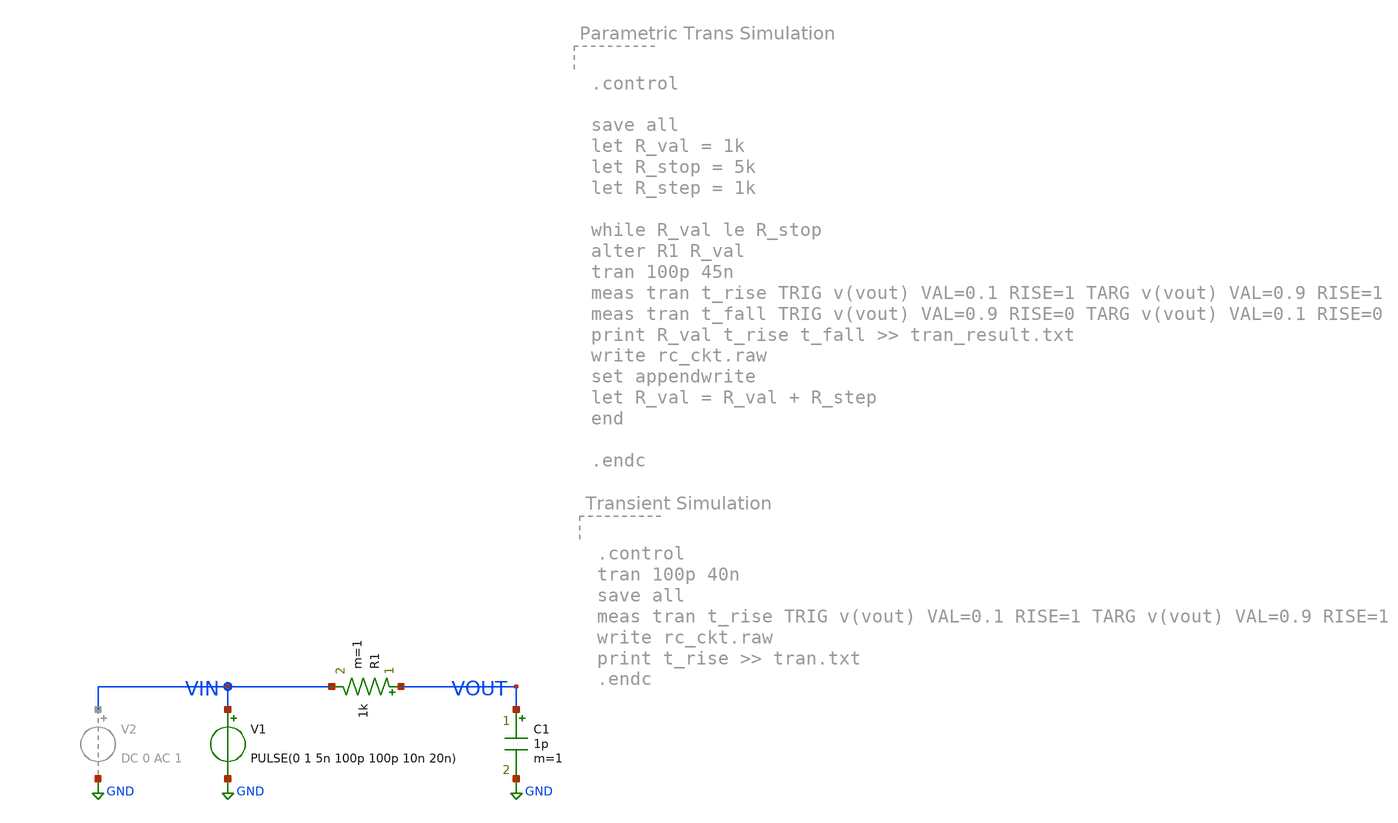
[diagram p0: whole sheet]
** sch_path: ITI_Labs/Lab1/RC/Design/RC.sch
**.subckt RC
C1 VOUT GND 1p m=1
R1 VOUT VIN 1k m=1
V1 VIN GND PULSE(0 1 5n 100p 100p 10n 20n)
**** begin user architecture code


.control

save all

let R_val = 1k
let R_stop = 1meg
let R_mult = 10

while R_val le R_stop
alter R1 R_val
ac dec 10 1 10g

meas ac MAX_GAIN MAX vmag(vout) FROM=1 TO=10G
meas ac BW WHEN vmag(vout)=0.707 FALL=1

print MAX_GAIN BW >> ac_result.txt
write rc_ckt_2.raw
set appendwrite
let R_val = R_val * R_mult
end

.endc




.control
ac dec 10 1 10G
save all
meas ac MAX_GAIN MAX vmag(vout) from=1 to=10G
write rc_ckt_ac.raw
set appendwrite
print MAX_GAIN >> ac.txt
.endc


**** end user architecture code
**.ends
.GLOBAL GND
.end
